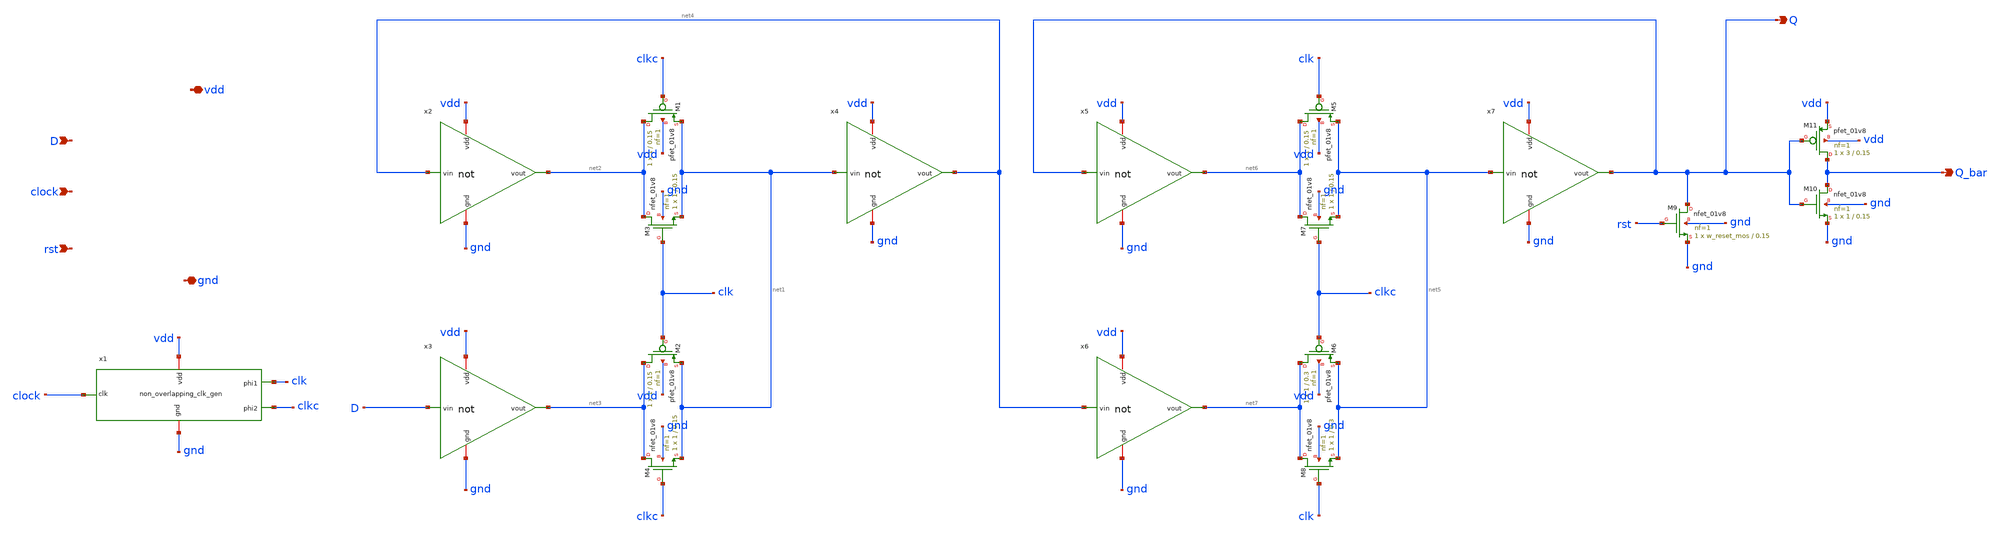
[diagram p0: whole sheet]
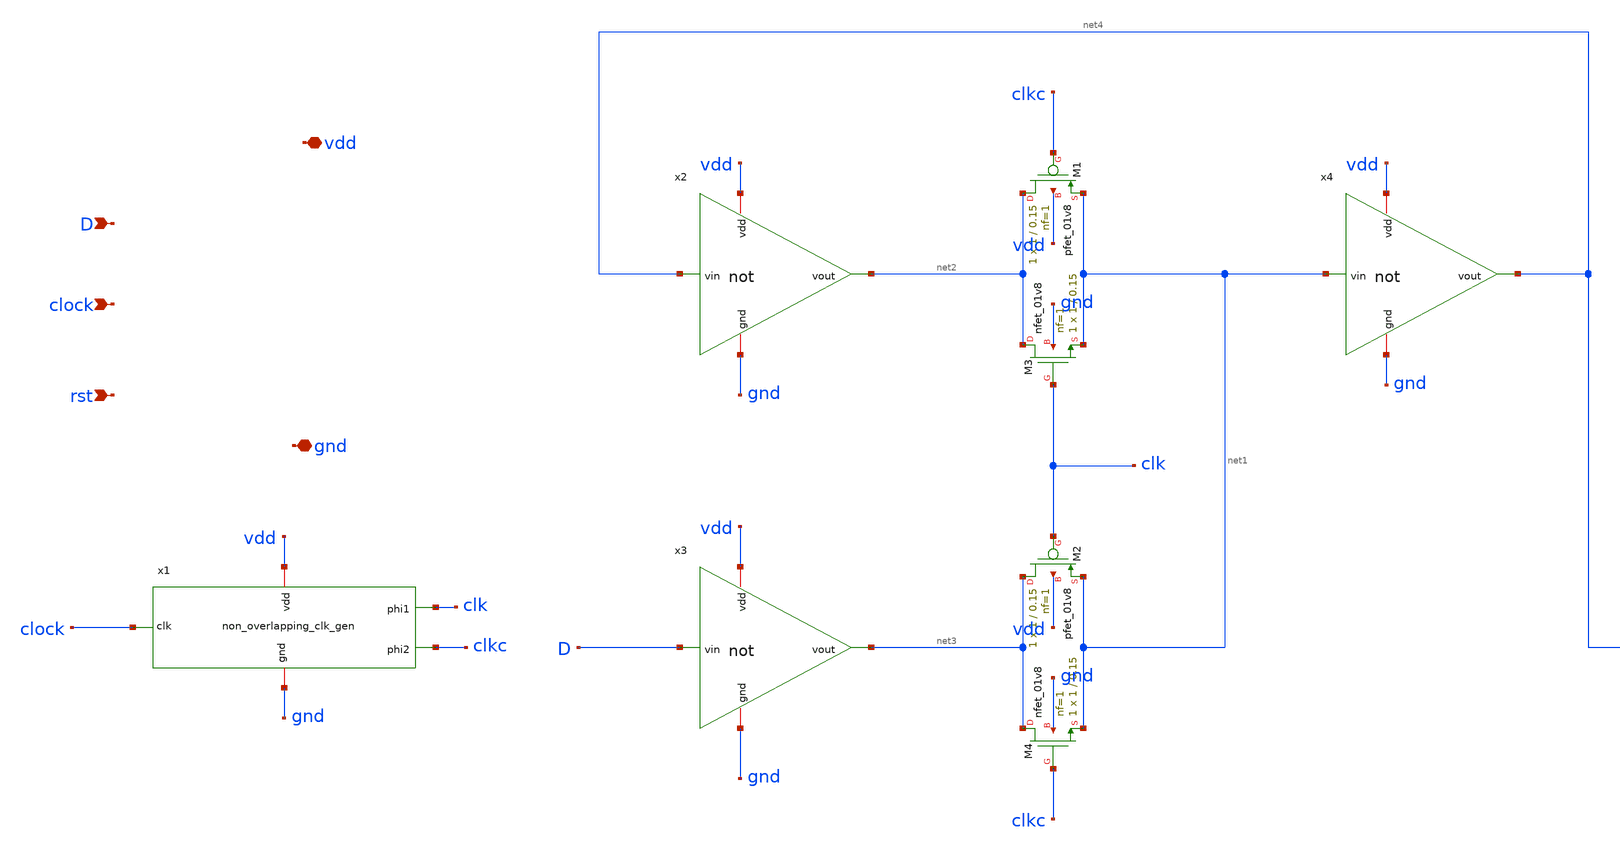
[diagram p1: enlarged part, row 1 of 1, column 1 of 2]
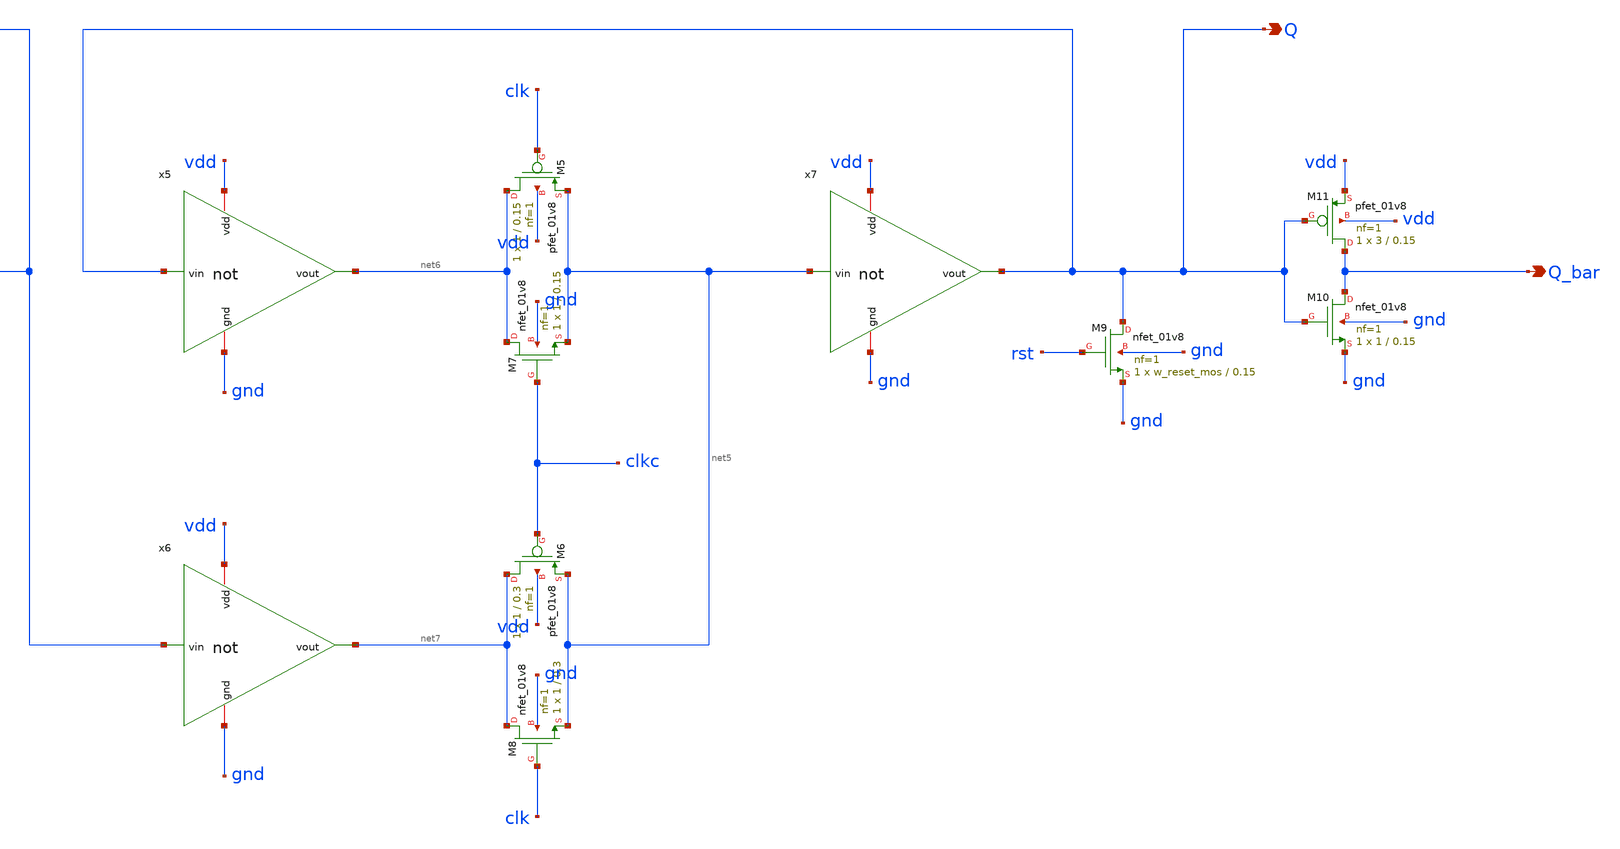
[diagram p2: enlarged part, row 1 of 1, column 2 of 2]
** sch_path: SequentialCircuits/D_ff/d_ff.sch
**.subckt d_ff D clock rst vdd gnd Q Q_bar
*.ipin D
*.ipin clock
*.ipin rst
*.iopin vdd
*.iopin gnd
*.opin Q
*.opin Q_bar
x2 vdd gnd net4 net2 not
x3 vdd gnd D net3 not
XM1 net2 clkc net1 vdd sky130_fd_pr__pfet_01v8 L=0.15 W=1 nf=1 ad='int((nf+1)/2) * W/nf * 0.29' as='int((nf+2)/2) * W/nf * 0.29'
+ pd='2*int((nf+1)/2) * (W/nf + 0.29)' ps='2*int((nf+2)/2) * (W/nf + 0.29)' nrd='0.29 / W' nrs='0.29 / W'
+ sa=0 sb=0 sd=0 mult=1 m=1
XM2 net3 clk net1 vdd sky130_fd_pr__pfet_01v8 L=0.15 W=1 nf=1 ad='int((nf+1)/2) * W/nf * 0.29' as='int((nf+2)/2) * W/nf * 0.29'
+ pd='2*int((nf+1)/2) * (W/nf + 0.29)' ps='2*int((nf+2)/2) * (W/nf + 0.29)' nrd='0.29 / W' nrs='0.29 / W'
+ sa=0 sb=0 sd=0 mult=1 m=1
XM3 net2 clk net1 gnd sky130_fd_pr__nfet_01v8 L=0.15 W=1 nf=1 ad='int((nf+1)/2) * W/nf * 0.29' as='int((nf+2)/2) * W/nf * 0.29'
+ pd='2*int((nf+1)/2) * (W/nf + 0.29)' ps='2*int((nf+2)/2) * (W/nf + 0.29)' nrd='0.29 / W' nrs='0.29 / W'
+ sa=0 sb=0 sd=0 mult=1 m=1
XM4 net3 clkc net1 gnd sky130_fd_pr__nfet_01v8 L=0.15 W=1 nf=1 ad='int((nf+1)/2) * W/nf * 0.29' as='int((nf+2)/2) * W/nf * 0.29'
+ pd='2*int((nf+1)/2) * (W/nf + 0.29)' ps='2*int((nf+2)/2) * (W/nf + 0.29)' nrd='0.29 / W' nrs='0.29 / W'
+ sa=0 sb=0 sd=0 mult=1 m=1
x4 vdd gnd net1 net4 not
x5 vdd gnd Q net6 not
x6 vdd gnd net4 net7 not
XM5 net6 clk net5 vdd sky130_fd_pr__pfet_01v8 L=0.15 W=1 nf=1 ad='int((nf+1)/2) * W/nf * 0.29' as='int((nf+2)/2) * W/nf * 0.29'
+ pd='2*int((nf+1)/2) * (W/nf + 0.29)' ps='2*int((nf+2)/2) * (W/nf + 0.29)' nrd='0.29 / W' nrs='0.29 / W'
+ sa=0 sb=0 sd=0 mult=1 m=1
XM6 net7 clkc net5 vdd sky130_fd_pr__pfet_01v8 L=0.3 W=1 nf=1 ad='int((nf+1)/2) * W/nf * 0.29' as='int((nf+2)/2) * W/nf * 0.29'
+ pd='2*int((nf+1)/2) * (W/nf + 0.29)' ps='2*int((nf+2)/2) * (W/nf + 0.29)' nrd='0.29 / W' nrs='0.29 / W'
+ sa=0 sb=0 sd=0 mult=1 m=1
XM7 net6 clkc net5 gnd sky130_fd_pr__nfet_01v8 L=0.15 W=1 nf=1 ad='int((nf+1)/2) * W/nf * 0.29' as='int((nf+2)/2) * W/nf * 0.29'
+ pd='2*int((nf+1)/2) * (W/nf + 0.29)' ps='2*int((nf+2)/2) * (W/nf + 0.29)' nrd='0.29 / W' nrs='0.29 / W'
+ sa=0 sb=0 sd=0 mult=1 m=1
XM8 net7 clk net5 gnd sky130_fd_pr__nfet_01v8 L=0.3 W=1 nf=1 ad='int((nf+1)/2) * W/nf * 0.29' as='int((nf+2)/2) * W/nf * 0.29'
+ pd='2*int((nf+1)/2) * (W/nf + 0.29)' ps='2*int((nf+2)/2) * (W/nf + 0.29)' nrd='0.29 / W' nrs='0.29 / W'
+ sa=0 sb=0 sd=0 mult=1 m=1
x7 vdd gnd net5 Q not
XM9 Q rst gnd gnd sky130_fd_pr__nfet_01v8 L=0.15 W=w_reset_mos nf=1 ad='int((nf+1)/2) * W/nf * 0.29'
+ as='int((nf+2)/2) * W/nf * 0.29' pd='2*int((nf+1)/2) * (W/nf + 0.29)' ps='2*int((nf+2)/2) * (W/nf + 0.29)'
+ nrd='0.29 / W' nrs='0.29 / W' sa=0 sb=0 sd=0 mult=1 m=1
x1 vdd clk clock clkc gnd non_overlapping_clk_gen
XM10 Q_bar Q gnd gnd sky130_fd_pr__nfet_01v8 L=0.15 W=1 nf=1 ad='int((nf+1)/2) * W/nf * 0.29' as='int((nf+2)/2) * W/nf * 0.29'
+ pd='2*int((nf+1)/2) * (W/nf + 0.29)' ps='2*int((nf+2)/2) * (W/nf + 0.29)' nrd='0.29 / W' nrs='0.29 / W'
+ sa=0 sb=0 sd=0 mult=1 m=1
XM11 Q_bar Q vdd vdd sky130_fd_pr__pfet_01v8 L=0.15 W=3 nf=1 ad='int((nf+1)/2) * W/nf * 0.29' as='int((nf+2)/2) * W/nf * 0.29'
+ pd='2*int((nf+1)/2) * (W/nf + 0.29)' ps='2*int((nf+2)/2) * (W/nf + 0.29)' nrd='0.29 / W' nrs='0.29 / W'
+ sa=0 sb=0 sd=0 mult=1 m=1
**.ends

* expanding   symbol:  LogicGates/not.sym # of pins=4
** sym_path: LogicGates/not.sym
** sch_path: LogicGates/not.sch
.subckt not vdd gnd vin vout
*.ipin vin
*.iopin vdd
*.iopin gnd
*.opin vout
XM2 vout vin vdd vdd sky130_fd_pr__pfet_01v8 L=0.15 W=2 nf=1 ad='int((nf+1)/2) * W/nf * 0.29' as='int((nf+2)/2) * W/nf * 0.29'
+ pd='2*int((nf+1)/2) * (W/nf + 0.29)' ps='2*int((nf+2)/2) * (W/nf + 0.29)' nrd='0.29 / W' nrs='0.29 / W'
+ sa=0 sb=0 sd=0 mult=1 m=1
XM1 vout vin gnd gnd sky130_fd_pr__nfet_01v8 L=0.15 W=1 nf=1 ad='int((nf+1)/2) * W/nf * 0.29' as='int((nf+2)/2) * W/nf * 0.29'
+ pd='2*int((nf+1)/2) * (W/nf + 0.29)' ps='2*int((nf+2)/2) * (W/nf + 0.29)' nrd='0.29 / W' nrs='0.29 / W'
+ sa=0 sb=0 sd=0 mult=1 m=1
.ends


* expanding   symbol:  SequentialCircuits/Non Overlapping Clock
*+ Generator/non_overlapping_clk_gen.sym # of pins=5
** sym_path: SequentialCircuits/Non Overlapping Clock Generator/non_overlapping_clk_gen.sym
** sch_path: SequentialCircuits/Non Overlapping Clock Generator/non_overlapping_clk_gen.sch
.subckt non_overlapping_clk_gen vdd phi1 clk phi2 gnd
*.ipin clk
*.iopin vdd
*.iopin gnd
*.opin phi1
*.opin phi2
x1 vdd gnd clk net1 not
x2 vdd gnd net1 phi2 phi1 nor
x3 vdd gnd phi1 clk phi2 nor
.ends


* expanding   symbol:  LogicGates/nor.sym # of pins=5
** sym_path: LogicGates/nor.sym
** sch_path: LogicGates/nor.sch
.subckt nor vdd gnd A B Y
*.ipin A
*.ipin B
*.iopin vdd
*.iopin gnd
*.opin Y
XM1 Y A gnd gnd sky130_fd_pr__nfet_01v8 L=0.15 W=1 nf=1 ad='int((nf+1)/2) * W/nf * 0.29' as='int((nf+2)/2) * W/nf * 0.29'
+ pd='2*int((nf+1)/2) * (W/nf + 0.29)' ps='2*int((nf+2)/2) * (W/nf + 0.29)' nrd='0.29 / W' nrs='0.29 / W'
+ sa=0 sb=0 sd=0 mult=1 m=1
XM2 Y B gnd gnd sky130_fd_pr__nfet_01v8 L=0.15 W=1 nf=1 ad='int((nf+1)/2) * W/nf * 0.29' as='int((nf+2)/2) * W/nf * 0.29'
+ pd='2*int((nf+1)/2) * (W/nf + 0.29)' ps='2*int((nf+2)/2) * (W/nf + 0.29)' nrd='0.29 / W' nrs='0.29 / W'
+ sa=0 sb=0 sd=0 mult=1 m=1
XM3 net1 A vdd vdd sky130_fd_pr__pfet_01v8 L=0.15 W=2 nf=1 ad='int((nf+1)/2) * W/nf * 0.29' as='int((nf+2)/2) * W/nf * 0.29'
+ pd='2*int((nf+1)/2) * (W/nf + 0.29)' ps='2*int((nf+2)/2) * (W/nf + 0.29)' nrd='0.29 / W' nrs='0.29 / W'
+ sa=0 sb=0 sd=0 mult=1 m=1
XM4 Y B net1 vdd sky130_fd_pr__pfet_01v8 L=0.15 W=2 nf=1 ad='int((nf+1)/2) * W/nf * 0.29' as='int((nf+2)/2) * W/nf * 0.29'
+ pd='2*int((nf+1)/2) * (W/nf + 0.29)' ps='2*int((nf+2)/2) * (W/nf + 0.29)' nrd='0.29 / W' nrs='0.29 / W'
+ sa=0 sb=0 sd=0 mult=1 m=1
.ends

.end
